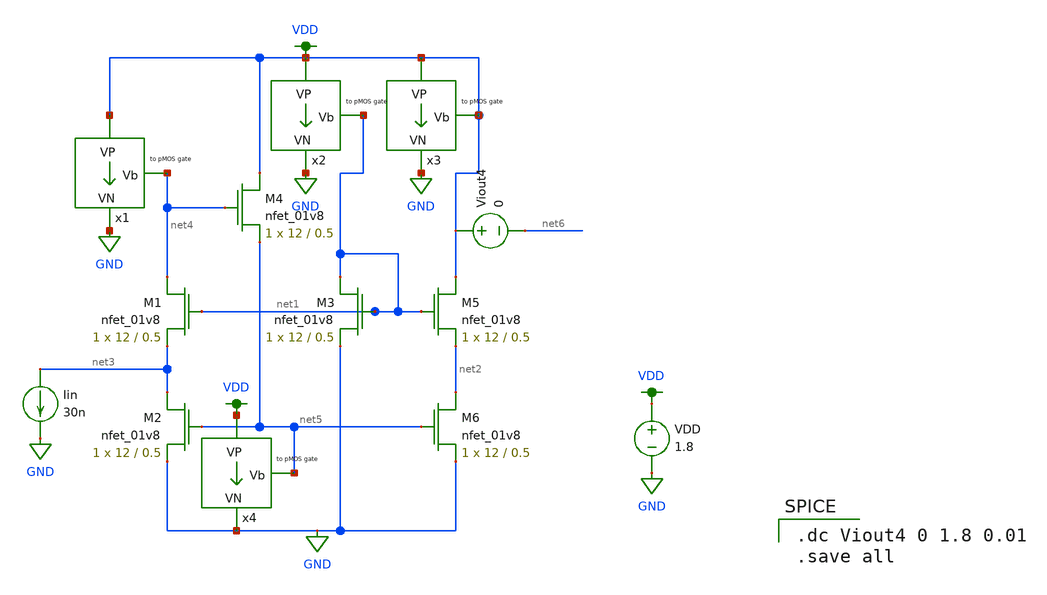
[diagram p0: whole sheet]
** sch_path: schematics/bias/low_voltage_flipped_voltage follower_current_mirror_2.sch
**.subckt low_voltage_flipped_voltage follower_current_mirror_2
XM1 net4 net1 net3 GND sky130_fd_pr__nfet_01v8 L=0.5 W=12 nf=1 ad='int((nf+1)/2) * W/nf * 0.29' as='int((nf+2)/2) * W/nf * 0.29'
+ pd='2*int((nf+1)/2) * (W/nf + 0.29)' ps='2*int((nf+2)/2) * (W/nf + 0.29)' nrd='0.29 / W' nrs='0.29 / W'
+ sa=0 sb=0 sd=0 mult=1 m=1
XM2 net3 net5 GND GND sky130_fd_pr__nfet_01v8 L=0.5 W=12 nf=1 ad='int((nf+1)/2) * W/nf * 0.29' as='int((nf+2)/2) * W/nf * 0.29'
+ pd='2*int((nf+1)/2) * (W/nf + 0.29)' ps='2*int((nf+2)/2) * (W/nf + 0.29)' nrd='0.29 / W' nrs='0.29 / W'
+ sa=0 sb=0 sd=0 mult=1 m=1
XM3 net1 net1 GND GND sky130_fd_pr__nfet_01v8 L=0.5 W=12 nf=1 ad='int((nf+1)/2) * W/nf * 0.29' as='int((nf+2)/2) * W/nf * 0.29'
+ pd='2*int((nf+1)/2) * (W/nf + 0.29)' ps='2*int((nf+2)/2) * (W/nf + 0.29)' nrd='0.29 / W' nrs='0.29 / W'
+ sa=0 sb=0 sd=0 mult=1 m=1
XM4 VDD net4 net5 GND sky130_fd_pr__nfet_01v8 L=0.5 W=12 nf=1 ad='int((nf+1)/2) * W/nf * 0.29' as='int((nf+2)/2) * W/nf * 0.29'
+ pd='2*int((nf+1)/2) * (W/nf + 0.29)' ps='2*int((nf+2)/2) * (W/nf + 0.29)' nrd='0.29 / W' nrs='0.29 / W'
+ sa=0 sb=0 sd=0 mult=1 m=1
XM5 VDD net1 net2 GND sky130_fd_pr__nfet_01v8 L=0.5 W=12 nf=1 ad='int((nf+1)/2) * W/nf * 0.29' as='int((nf+2)/2) * W/nf * 0.29'
+ pd='2*int((nf+1)/2) * (W/nf + 0.29)' ps='2*int((nf+2)/2) * (W/nf + 0.29)' nrd='0.29 / W' nrs='0.29 / W'
+ sa=0 sb=0 sd=0 mult=1 m=1
XM6 net2 net5 GND GND sky130_fd_pr__nfet_01v8 L=0.5 W=12 nf=1 ad='int((nf+1)/2) * W/nf * 0.29' as='int((nf+2)/2) * W/nf * 0.29'
+ pd='2*int((nf+1)/2) * (W/nf + 0.29)' ps='2*int((nf+2)/2) * (W/nf + 0.29)' nrd='0.29 / W' nrs='0.29 / W'
+ sa=0 sb=0 sd=0 mult=1 m=1
Viout4 VDD net6 0
Iin net3 GND 30n
VDD VDD GND 1.8
x1 VDD net4 GND current_bias
x2 VDD net1 GND current_bias
x3 VDD VDD GND current_bias
x4 VDD net5 GND current_bias
**** begin user architecture code

.option wnflag=1
.param MC_SWITCH=0.0
.lib ~/skywater/skywater-pdk/libraries/sky130_fd_pr_ngspice/latest/models/sky130.lib.spice tt


.dc Viout4 0 1.8 0.01
.save all

**** end user architecture code
**.ends

* expanding   symbol:
*+  /home/madvlsi/dev/git/7-bit-D-A-converter-MP4-MADVLSI/schematics/bias/current_bias.sym # of pins=3
** sym_path: schematics/bias_2/current_bias.sym
** sch_path: schematics/bias_2/current_bias.sch
.subckt current_bias VP Vb VN
*.iopin VP
*.iopin VN
*.opin Vb
XM4 net1 net1 net4 GND sky130_fd_pr__nfet_01v8 L=0.5 W=12 nf=1 ad='int((nf+1)/2) * W/nf * 0.29' as='int((nf+2)/2) * W/nf * 0.29'
+ pd='2*int((nf+1)/2) * (W/nf + 0.29)' ps='2*int((nf+2)/2) * (W/nf + 0.29)' nrd='0.29 / W' nrs='0.29 / W'
+ sa=0 sb=0 sd=0 mult=8 m=8
XM5 net3 net1 VN GND sky130_fd_pr__nfet_01v8 L=0.5 W=12 nf=1 ad='int((nf+1)/2) * W/nf * 0.29' as='int((nf+2)/2) * W/nf * 0.29'
+ pd='2*int((nf+1)/2) * (W/nf + 0.29)' ps='2*int((nf+2)/2) * (W/nf + 0.29)' nrd='0.29 / W' nrs='0.29 / W'
+ sa=0 sb=0 sd=0 mult=1 m=1
XM6 Vb net2 VN GND sky130_fd_pr__nfet_01v8 L=0.5 W=12 nf=1 ad='int((nf+1)/2) * W/nf * 0.29' as='int((nf+2)/2) * W/nf * 0.29'
+ pd='2*int((nf+1)/2) * (W/nf + 0.29)' ps='2*int((nf+2)/2) * (W/nf + 0.29)' nrd='0.29 / W' nrs='0.29 / W'
+ sa=0 sb=0 sd=0 mult=1 m=1
XM7 net2 net2 VN GND sky130_fd_pr__nfet_01v8 L=0.5 W=12 nf=1 ad='int((nf+1)/2) * W/nf * 0.29' as='int((nf+2)/2) * W/nf * 0.29'
+ pd='2*int((nf+1)/2) * (W/nf + 0.29)' ps='2*int((nf+2)/2) * (W/nf + 0.29)' nrd='0.29 / W' nrs='0.29 / W'
+ sa=0 sb=0 sd=0 mult=1 m=1
R1 net4 VN 100k m=1
XM8 Vb net3 VP VDD sky130_fd_pr__pfet_01v8 L=0.5 W=12 nf=1 ad='int((nf+1)/2) * W/nf * 0.29' as='int((nf+2)/2) * W/nf * 0.29'
+ pd='2*int((nf+1)/2) * (W/nf + 0.29)' ps='2*int((nf+2)/2) * (W/nf + 0.29)' nrd='0.29 / W' nrs='0.29 / W'
+ sa=0 sb=0 sd=0 mult=1 m=1
XM9 net2 Vb VP VDD sky130_fd_pr__pfet_01v8 L=0.5 W=12 nf=1 ad='int((nf+1)/2) * W/nf * 0.29' as='int((nf+2)/2) * W/nf * 0.29'
+ pd='2*int((nf+1)/2) * (W/nf + 0.29)' ps='2*int((nf+2)/2) * (W/nf + 0.29)' nrd='0.29 / W' nrs='0.29 / W'
+ sa=0 sb=0 sd=0 mult=1 m=1
XM10 net3 net3 VP VDD sky130_fd_pr__pfet_01v8 L=0.5 W=12 nf=1 ad='int((nf+1)/2) * W/nf * 0.29' as='int((nf+2)/2) * W/nf * 0.29'
+ pd='2*int((nf+1)/2) * (W/nf + 0.29)' ps='2*int((nf+2)/2) * (W/nf + 0.29)' nrd='0.29 / W' nrs='0.29 / W'
+ sa=0 sb=0 sd=0 mult=1 m=1
XM11 net1 Vb VP VDD sky130_fd_pr__pfet_01v8 L=0.5 W=12 nf=1 ad='int((nf+1)/2) * W/nf * 0.29' as='int((nf+2)/2) * W/nf * 0.29'
+ pd='2*int((nf+1)/2) * (W/nf + 0.29)' ps='2*int((nf+2)/2) * (W/nf + 0.29)' nrd='0.29 / W' nrs='0.29 / W'
+ sa=0 sb=0 sd=0 mult=1 m=1
.ends

.GLOBAL GND
.GLOBAL VDD
.end
